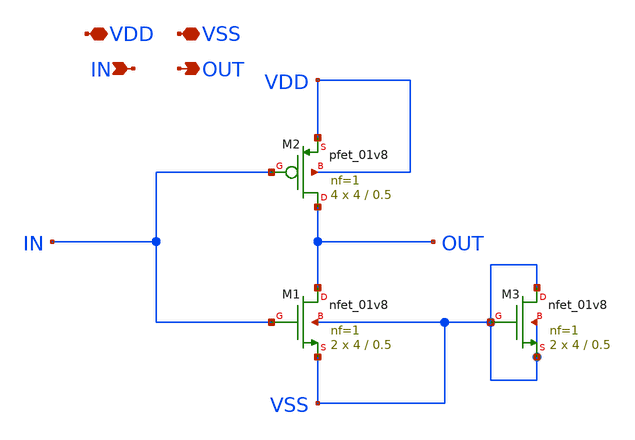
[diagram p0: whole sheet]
** sch_path: xschem/INV_1.sch
**.subckt INV_1 VDD VSS IN OUT
*.iopin VDD
*.iopin VSS
*.ipin IN
*.opin OUT
XM1 OUT IN VSS VSS sky130_fd_pr__nfet_01v8 L=0.5 W=4 nf=1 ad='int((nf+1)/2) * W/nf * 0.29' as='int((nf+2)/2) * W/nf * 0.29'
+ pd='2*int((nf+1)/2) * (W/nf + 0.29)' ps='2*int((nf+2)/2) * (W/nf + 0.29)' nrd='0.29 / W' nrs='0.29 / W'
+ sa=0 sb=0 sd=0 mult=2 m=2
XM2 OUT IN VDD VDD sky130_fd_pr__pfet_01v8 L=0.5 W=4 nf=1 ad='int((nf+1)/2) * W/nf * 0.29' as='int((nf+2)/2) * W/nf * 0.29'
+ pd='2*int((nf+1)/2) * (W/nf + 0.29)' ps='2*int((nf+2)/2) * (W/nf + 0.29)' nrd='0.29 / W' nrs='0.29 / W'
+ sa=0 sb=0 sd=0 mult=4 m=4
XM3 VSS VSS VSS VSS sky130_fd_pr__nfet_01v8 L=0.5 W=4 nf=1 ad='int((nf+1)/2) * W/nf * 0.29' as='int((nf+2)/2) * W/nf * 0.29'
+ pd='2*int((nf+1)/2) * (W/nf + 0.29)' ps='2*int((nf+2)/2) * (W/nf + 0.29)' nrd='0.29 / W' nrs='0.29 / W'
+ sa=0 sb=0 sd=0 mult=2 m=2
**.ends
.end
